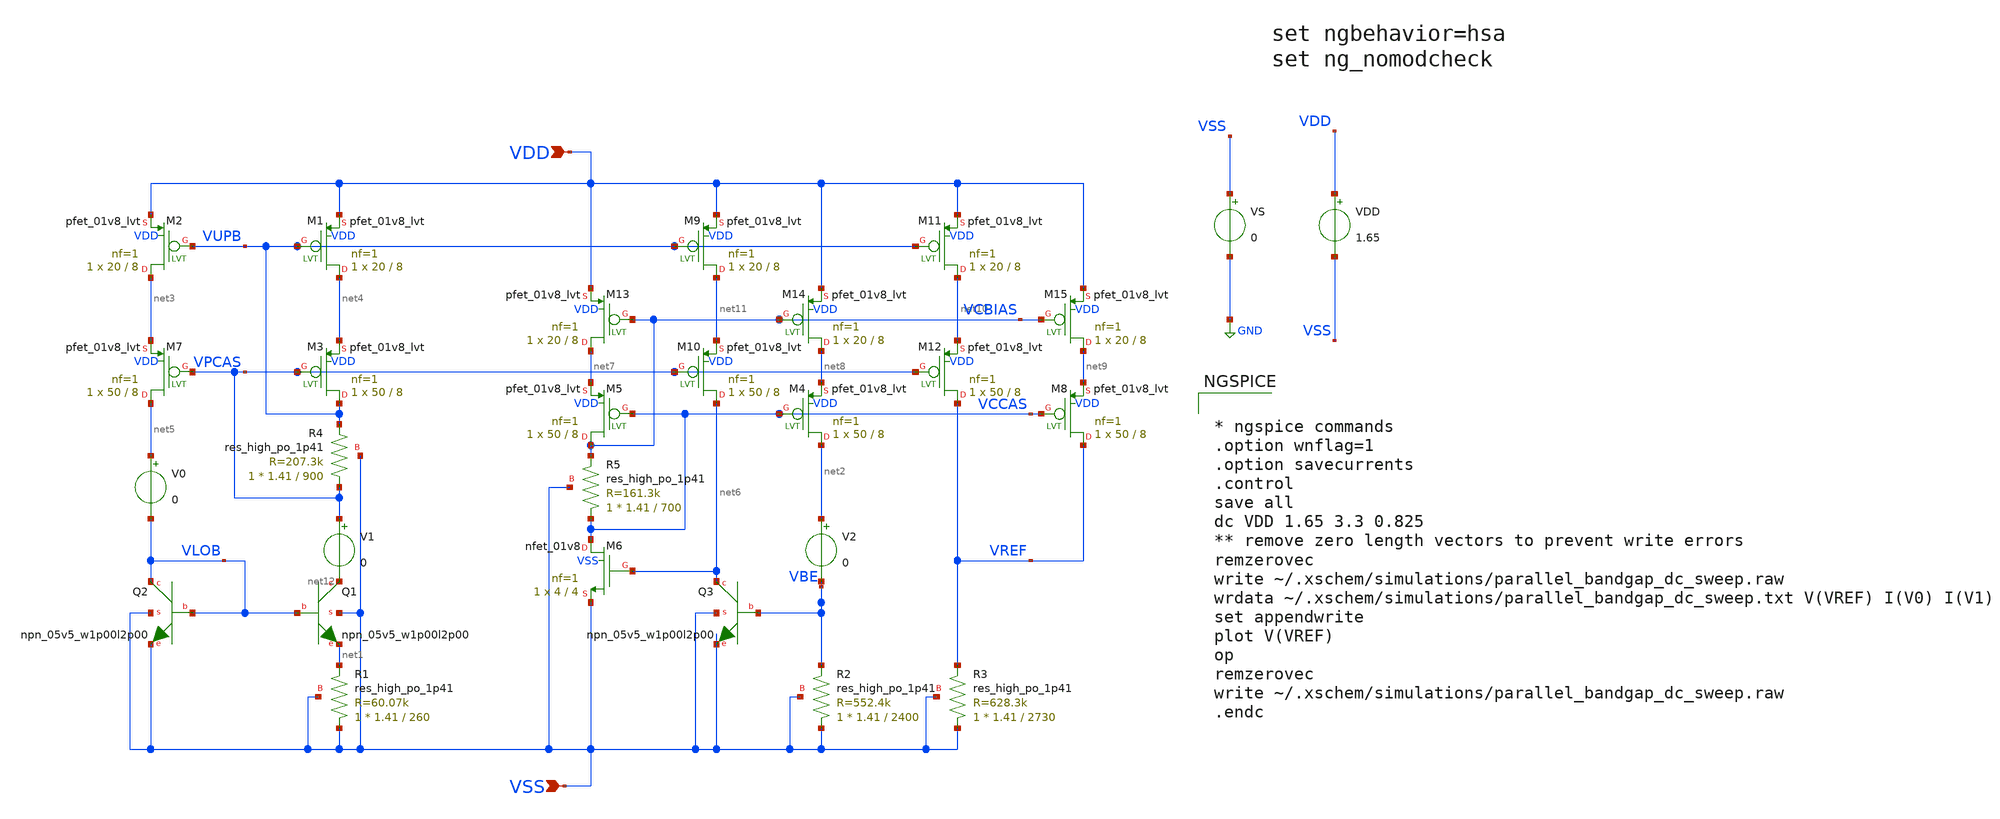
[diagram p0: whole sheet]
** sch_path: designs/parallel_bandgap_dc_sweep.sch
**.subckt parallel_bandgap_dc_sweep VDD VSS
*.ipin VDD
*.ipin VSS
XM1 net4 VUPB VDD VDD sky130_fd_pr__pfet_01v8_lvt L=8 W=20 nf=1 ad='int((nf+1)/2) * W/nf * 0.29' as='int((nf+2)/2) * W/nf * 0.29'
+ pd='2*int((nf+1)/2) * (W/nf + 0.29)' ps='2*int((nf+2)/2) * (W/nf + 0.29)' nrd='0.29 / W' nrs='0.29 / W'
+ sa=0 sb=0 sd=0 mult=1 m=1
XM2 net3 VUPB VDD VDD sky130_fd_pr__pfet_01v8_lvt L=8 W=20 nf=1 ad='int((nf+1)/2) * W/nf * 0.29' as='int((nf+2)/2) * W/nf * 0.29'
+ pd='2*int((nf+1)/2) * (W/nf + 0.29)' ps='2*int((nf+2)/2) * (W/nf + 0.29)' nrd='0.29 / W' nrs='0.29 / W'
+ sa=0 sb=0 sd=0 mult=1 m=1
XQ1 net12 VLOB net1 VSS sky130_fd_pr__npn_05v5_w1p00l2p00
XQ2 VLOB VLOB VSS VSS sky130_fd_pr__npn_05v5_w1p00l2p00
XR1 VSS net1 VSS sky130_fd_pr__res_high_po_1p41 L=260 mult=1 m=1
XQ3 net6 VBE VSS VSS sky130_fd_pr__npn_05v5_w1p00l2p00
XR2 VSS VBE VSS sky130_fd_pr__res_high_po_1p41 L=2400 mult=1 m=1
XM4 net2 VCCAS net8 VDD sky130_fd_pr__pfet_01v8_lvt L=8 W=50 nf=1 ad='int((nf+1)/2) * W/nf * 0.29' as='int((nf+2)/2) * W/nf * 0.29'
+ pd='2*int((nf+1)/2) * (W/nf + 0.29)' ps='2*int((nf+2)/2) * (W/nf + 0.29)' nrd='0.29 / W' nrs='0.29 / W'
+ sa=0 sb=0 sd=0 mult=1 m=1
XM5 VCBIAS VCCAS net7 VDD sky130_fd_pr__pfet_01v8_lvt L=8 W=50 nf=1 ad='int((nf+1)/2) * W/nf * 0.29'
+ as='int((nf+2)/2) * W/nf * 0.29' pd='2*int((nf+1)/2) * (W/nf + 0.29)' ps='2*int((nf+2)/2) * (W/nf + 0.29)'
+ nrd='0.29 / W' nrs='0.29 / W' sa=0 sb=0 sd=0 mult=1 m=1
XM6 VCCAS net6 VSS VSS sky130_fd_pr__nfet_01v8 L=4 W=4 nf=1 ad='int((nf+1)/2) * W/nf * 0.29' as='int((nf+2)/2) * W/nf * 0.29'
+ pd='2*int((nf+1)/2) * (W/nf + 0.29)' ps='2*int((nf+2)/2) * (W/nf + 0.29)' nrd='0.29 / W' nrs='0.29 / W'
+ sa=0 sb=0 sd=0 mult=1 m=1
XR3 VSS VREF VSS sky130_fd_pr__res_high_po_1p41 L=2730 mult=1 m=1
XM8 VREF VCCAS net9 VDD sky130_fd_pr__pfet_01v8_lvt L=8 W=50 nf=1 ad='int((nf+1)/2) * W/nf * 0.29' as='int((nf+2)/2) * W/nf * 0.29'
+ pd='2*int((nf+1)/2) * (W/nf + 0.29)' ps='2*int((nf+2)/2) * (W/nf + 0.29)' nrd='0.29 / W' nrs='0.29 / W'
+ sa=0 sb=0 sd=0 mult=1 m=1
VDD VDD VSS 1.65
.save i(vdd)
VS VSS GND 0
V0 net5 VLOB 0
.save i(v0)
V2 net2 VBE 0
.save i(v2)
V1 VPCAS net12 0
.save i(v1)
XM3 VUPB VPCAS net4 VDD sky130_fd_pr__pfet_01v8_lvt L=8 W=50 nf=1 ad='int((nf+1)/2) * W/nf * 0.29' as='int((nf+2)/2) * W/nf * 0.29'
+ pd='2*int((nf+1)/2) * (W/nf + 0.29)' ps='2*int((nf+2)/2) * (W/nf + 0.29)' nrd='0.29 / W' nrs='0.29 / W'
+ sa=0 sb=0 sd=0 mult=1 m=1
XM7 net5 VPCAS net3 VDD sky130_fd_pr__pfet_01v8_lvt L=8 W=50 nf=1 ad='int((nf+1)/2) * W/nf * 0.29' as='int((nf+2)/2) * W/nf * 0.29'
+ pd='2*int((nf+1)/2) * (W/nf + 0.29)' ps='2*int((nf+2)/2) * (W/nf + 0.29)' nrd='0.29 / W' nrs='0.29 / W'
+ sa=0 sb=0 sd=0 mult=1 m=1
XR4 VPCAS VUPB VSS sky130_fd_pr__res_high_po_1p41 L=900 mult=1 m=1
XM9 net11 VUPB VDD VDD sky130_fd_pr__pfet_01v8_lvt L=8 W=20 nf=1 ad='int((nf+1)/2) * W/nf * 0.29' as='int((nf+2)/2) * W/nf * 0.29'
+ pd='2*int((nf+1)/2) * (W/nf + 0.29)' ps='2*int((nf+2)/2) * (W/nf + 0.29)' nrd='0.29 / W' nrs='0.29 / W'
+ sa=0 sb=0 sd=0 mult=1 m=1
XM10 net6 VPCAS net11 VDD sky130_fd_pr__pfet_01v8_lvt L=8 W=50 nf=1 ad='int((nf+1)/2) * W/nf * 0.29'
+ as='int((nf+2)/2) * W/nf * 0.29' pd='2*int((nf+1)/2) * (W/nf + 0.29)' ps='2*int((nf+2)/2) * (W/nf + 0.29)'
+ nrd='0.29 / W' nrs='0.29 / W' sa=0 sb=0 sd=0 mult=1 m=1
XM11 net10 VUPB VDD VDD sky130_fd_pr__pfet_01v8_lvt L=8 W=20 nf=1 ad='int((nf+1)/2) * W/nf * 0.29' as='int((nf+2)/2) * W/nf * 0.29'
+ pd='2*int((nf+1)/2) * (W/nf + 0.29)' ps='2*int((nf+2)/2) * (W/nf + 0.29)' nrd='0.29 / W' nrs='0.29 / W'
+ sa=0 sb=0 sd=0 mult=1 m=1
XM12 VREF VPCAS net10 VDD sky130_fd_pr__pfet_01v8_lvt L=8 W=50 nf=1 ad='int((nf+1)/2) * W/nf * 0.29'
+ as='int((nf+2)/2) * W/nf * 0.29' pd='2*int((nf+1)/2) * (W/nf + 0.29)' ps='2*int((nf+2)/2) * (W/nf + 0.29)'
+ nrd='0.29 / W' nrs='0.29 / W' sa=0 sb=0 sd=0 mult=1 m=1
XM13 net7 VCBIAS VDD VDD sky130_fd_pr__pfet_01v8_lvt L=8 W=20 nf=1 ad='int((nf+1)/2) * W/nf * 0.29' as='int((nf+2)/2) * W/nf * 0.29'
+ pd='2*int((nf+1)/2) * (W/nf + 0.29)' ps='2*int((nf+2)/2) * (W/nf + 0.29)' nrd='0.29 / W' nrs='0.29 / W'
+ sa=0 sb=0 sd=0 mult=1 m=1
XM14 net8 VCBIAS VDD VDD sky130_fd_pr__pfet_01v8_lvt L=8 W=20 nf=1 ad='int((nf+1)/2) * W/nf * 0.29' as='int((nf+2)/2) * W/nf * 0.29'
+ pd='2*int((nf+1)/2) * (W/nf + 0.29)' ps='2*int((nf+2)/2) * (W/nf + 0.29)' nrd='0.29 / W' nrs='0.29 / W'
+ sa=0 sb=0 sd=0 mult=1 m=1
XR5 VCCAS VCBIAS VSS sky130_fd_pr__res_high_po_1p41 L=700 mult=1 m=1
XM15 net9 VCBIAS VDD VDD sky130_fd_pr__pfet_01v8_lvt L=8 W=20 nf=1 ad='int((nf+1)/2) * W/nf * 0.29' as='int((nf+2)/2) * W/nf * 0.29'
+ pd='2*int((nf+1)/2) * (W/nf + 0.29)' ps='2*int((nf+2)/2) * (W/nf + 0.29)' nrd='0.29 / W' nrs='0.29 / W'
+ sa=0 sb=0 sd=0 mult=1 m=1
**** begin user architecture code


* ngspice commands
.option wnflag=1
.option savecurrents
.control
save all
dc VDD 1.65 3.3 0.825
** remove zero length vectors to prevent write errors
remzerovec
write ~/.xschem/simulations/parallel_bandgap_dc_sweep.raw
wrdata ~/.xschem/simulations/parallel_bandgap_dc_sweep.txt V(VREF) I(V0) I(V1)
set appendwrite
plot V(VREF)
op
remzerovec
write ~/.xschem/simulations/parallel_bandgap_dc_sweep.raw
.endc



** opencircuitdesign pdks install
.lib /foss/pdks/sky130A/libs.tech/ngspice/sky130.lib.corners.spice tt

**** end user architecture code
**.ends
.GLOBAL GND
.end
